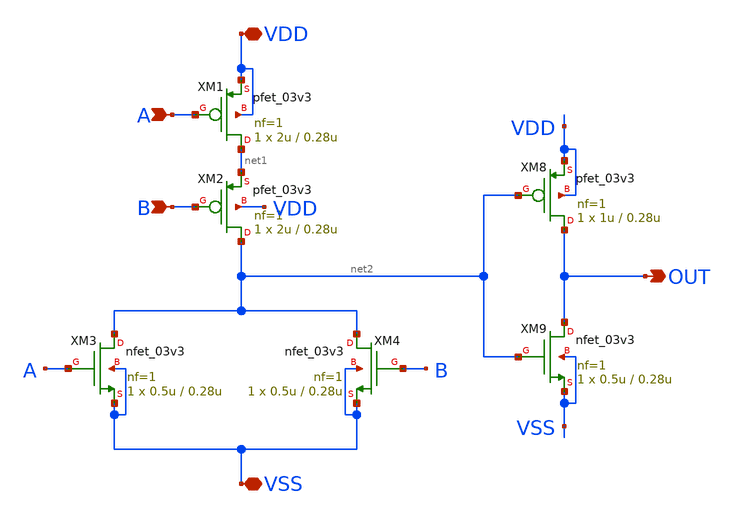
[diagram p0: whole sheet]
** sch_path: SCOP_INPUT_AND_MUX_PAKISTAN_03/Xschem/Logic_Gates/OR_2_Input.sch
**.subckt OR_2_Input A B VDD VSS OUT
*.ipin A
*.ipin B
*.iopin VDD
*.iopin VSS
*.opin OUT
XM1 net1 A VDD VDD pfet_03v3 L=0.28u W=2u nf=1 ad='int((nf+1)/2) * W/nf * 0.18u' as='int((nf+2)/2) * W/nf * 0.18u'
+ pd='2*int((nf+1)/2) * (W/nf + 0.18u)' ps='2*int((nf+2)/2) * (W/nf + 0.18u)' nrd='0.18u / W' nrs='0.18u / W'
+ sa=0 sb=0 sd=0 m=1
XM2 net2 B net1 VDD pfet_03v3 L=0.28u W=2u nf=1 ad='int((nf+1)/2) * W/nf * 0.18u' as='int((nf+2)/2) * W/nf * 0.18u'
+ pd='2*int((nf+1)/2) * (W/nf + 0.18u)' ps='2*int((nf+2)/2) * (W/nf + 0.18u)' nrd='0.18u / W' nrs='0.18u / W'
+ sa=0 sb=0 sd=0 m=1
XM3 net2 A VSS VSS nfet_03v3 L=0.28u W=0.5u nf=1 ad='int((nf+1)/2) * W/nf * 0.18u' as='int((nf+2)/2) * W/nf * 0.18u'
+ pd='2*int((nf+1)/2) * (W/nf + 0.18u)' ps='2*int((nf+2)/2) * (W/nf + 0.18u)' nrd='0.18u / W' nrs='0.18u / W'
+ sa=0 sb=0 sd=0 m=1
XM4 net2 B VSS VSS nfet_03v3 L=0.28u W=0.5u nf=1 ad='int((nf+1)/2) * W/nf * 0.18u' as='int((nf+2)/2) * W/nf * 0.18u'
+ pd='2*int((nf+1)/2) * (W/nf + 0.18u)' ps='2*int((nf+2)/2) * (W/nf + 0.18u)' nrd='0.18u / W' nrs='0.18u / W'
+ sa=0 sb=0 sd=0 m=1
XM8 OUT net2 VDD VDD pfet_03v3 L=0.28u W=1u nf=1 ad='int((nf+1)/2) * W/nf * 0.18u' as='int((nf+2)/2) * W/nf * 0.18u'
+ pd='2*int((nf+1)/2) * (W/nf + 0.18u)' ps='2*int((nf+2)/2) * (W/nf + 0.18u)' nrd='0.18u / W' nrs='0.18u / W'
+ sa=0 sb=0 sd=0 m=1
XM9 OUT net2 VSS VSS nfet_03v3 L=0.28u W=0.5u nf=1 ad='int((nf+1)/2) * W/nf * 0.18u' as='int((nf+2)/2) * W/nf * 0.18u'
+ pd='2*int((nf+1)/2) * (W/nf + 0.18u)' ps='2*int((nf+2)/2) * (W/nf + 0.18u)' nrd='0.18u / W' nrs='0.18u / W'
+ sa=0 sb=0 sd=0 m=1
**.ends
.end
